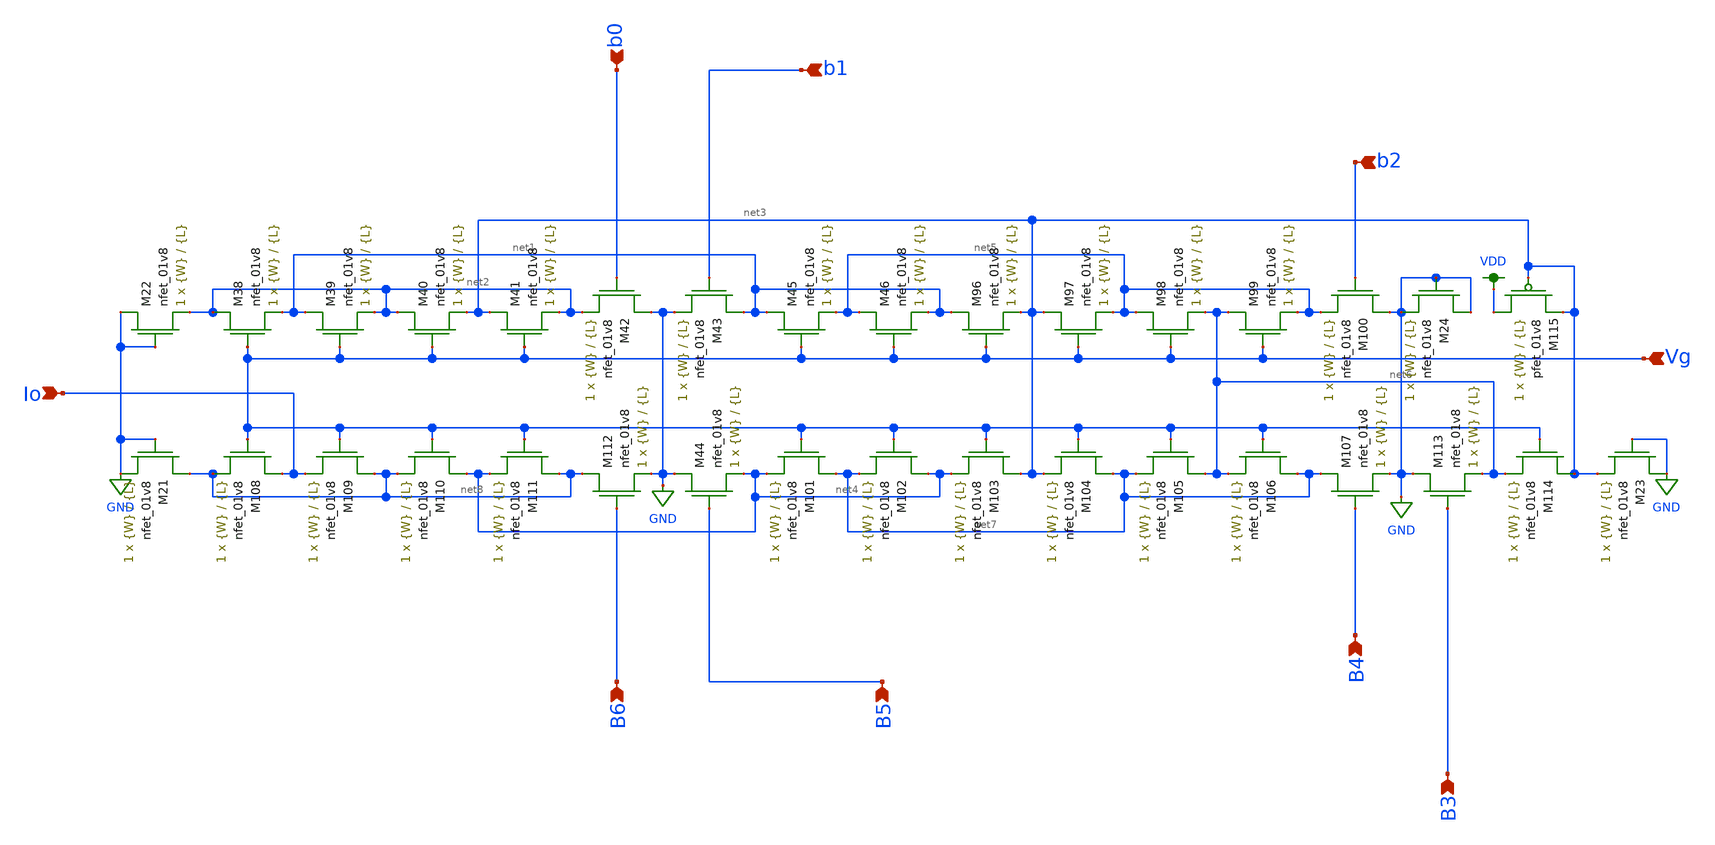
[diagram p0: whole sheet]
** sch_path: dac/schematics/misc/lvs_Dac.sch
**.subckt lvs_Dac b0 b1 b2 Vg B4 B3 B5 B6 Io
*.ipin b0
*.ipin b1
*.ipin b2
*.ipin Vg
*.ipin B4
*.ipin B3
*.ipin B5
*.ipin B6
*.ipin Io
XM38 net2 Vg net1 GND sky130_fd_pr__nfet_01v8 L={L} W={W} nf=1 ad='int((nf+1)/2) * W/nf * 0.29' as='int((nf+2)/2) * W/nf * 0.29'
+ pd='2*int((nf+1)/2) * (W/nf + 0.29)' ps='2*int((nf+2)/2) * (W/nf + 0.29)' nrd='0.29 / W' nrs='0.29 / W'
+ sa=0 sb=0 sd=0 mult=1 m=1
XM39 net1 Vg net2 GND sky130_fd_pr__nfet_01v8 L={L} W={W} nf=1 ad='int((nf+1)/2) * W/nf * 0.29' as='int((nf+2)/2) * W/nf * 0.29'
+ pd='2*int((nf+1)/2) * (W/nf + 0.29)' ps='2*int((nf+2)/2) * (W/nf + 0.29)' nrd='0.29 / W' nrs='0.29 / W'
+ sa=0 sb=0 sd=0 mult=1 m=1
XM40 net2 Vg net3 GND sky130_fd_pr__nfet_01v8 L={L} W={W} nf=1 ad='int((nf+1)/2) * W/nf * 0.29' as='int((nf+2)/2) * W/nf * 0.29'
+ pd='2*int((nf+1)/2) * (W/nf + 0.29)' ps='2*int((nf+2)/2) * (W/nf + 0.29)' nrd='0.29 / W' nrs='0.29 / W'
+ sa=0 sb=0 sd=0 mult=1 m=1
XM41 net3 Vg net2 GND sky130_fd_pr__nfet_01v8 L={L} W={W} nf=1 ad='int((nf+1)/2) * W/nf * 0.29' as='int((nf+2)/2) * W/nf * 0.29'
+ pd='2*int((nf+1)/2) * (W/nf + 0.29)' ps='2*int((nf+2)/2) * (W/nf + 0.29)' nrd='0.29 / W' nrs='0.29 / W'
+ sa=0 sb=0 sd=0 mult=1 m=1
XM42 GND b0 net2 GND sky130_fd_pr__nfet_01v8 L={L} W={W} nf=1 ad='int((nf+1)/2) * W/nf * 0.29' as='int((nf+2)/2) * W/nf * 0.29'
+ pd='2*int((nf+1)/2) * (W/nf + 0.29)' ps='2*int((nf+2)/2) * (W/nf + 0.29)' nrd='0.29 / W' nrs='0.29 / W'
+ sa=0 sb=0 sd=0 mult=1 m=1
XM43 net1 b1 GND GND sky130_fd_pr__nfet_01v8 L={L} W={W} nf=1 ad='int((nf+1)/2) * W/nf * 0.29' as='int((nf+2)/2) * W/nf * 0.29'
+ pd='2*int((nf+1)/2) * (W/nf + 0.29)' ps='2*int((nf+2)/2) * (W/nf + 0.29)' nrd='0.29 / W' nrs='0.29 / W'
+ sa=0 sb=0 sd=0 mult=1 m=1
XM44 GND B5 net4 GND sky130_fd_pr__nfet_01v8 L={L} W={W} nf=1 ad='int((nf+1)/2) * W/nf * 0.29' as='int((nf+2)/2) * W/nf * 0.29'
+ pd='2*int((nf+1)/2) * (W/nf + 0.29)' ps='2*int((nf+2)/2) * (W/nf + 0.29)' nrd='0.29 / W' nrs='0.29 / W'
+ sa=0 sb=0 sd=0 mult=1 m=1
XM45 net1 Vg net5 GND sky130_fd_pr__nfet_01v8 L={L} W={W} nf=1 ad='int((nf+1)/2) * W/nf * 0.29' as='int((nf+2)/2) * W/nf * 0.29'
+ pd='2*int((nf+1)/2) * (W/nf + 0.29)' ps='2*int((nf+2)/2) * (W/nf + 0.29)' nrd='0.29 / W' nrs='0.29 / W'
+ sa=0 sb=0 sd=0 mult=1 m=1
XM46 net5 Vg net1 GND sky130_fd_pr__nfet_01v8 L={L} W={W} nf=1 ad='int((nf+1)/2) * W/nf * 0.29' as='int((nf+2)/2) * W/nf * 0.29'
+ pd='2*int((nf+1)/2) * (W/nf + 0.29)' ps='2*int((nf+2)/2) * (W/nf + 0.29)' nrd='0.29 / W' nrs='0.29 / W'
+ sa=0 sb=0 sd=0 mult=1 m=1
XM96 net1 Vg net3 GND sky130_fd_pr__nfet_01v8 L={L} W={W} nf=1 ad='int((nf+1)/2) * W/nf * 0.29' as='int((nf+2)/2) * W/nf * 0.29'
+ pd='2*int((nf+1)/2) * (W/nf + 0.29)' ps='2*int((nf+2)/2) * (W/nf + 0.29)' nrd='0.29 / W' nrs='0.29 / W'
+ sa=0 sb=0 sd=0 mult=1 m=1
XM97 net3 Vg net5 GND sky130_fd_pr__nfet_01v8 L={L} W={W} nf=1 ad='int((nf+1)/2) * W/nf * 0.29' as='int((nf+2)/2) * W/nf * 0.29'
+ pd='2*int((nf+1)/2) * (W/nf + 0.29)' ps='2*int((nf+2)/2) * (W/nf + 0.29)' nrd='0.29 / W' nrs='0.29 / W'
+ sa=0 sb=0 sd=0 mult=1 m=1
XM98 net5 Vg net6 GND sky130_fd_pr__nfet_01v8 L={L} W={W} nf=1 ad='int((nf+1)/2) * W/nf * 0.29' as='int((nf+2)/2) * W/nf * 0.29'
+ pd='2*int((nf+1)/2) * (W/nf + 0.29)' ps='2*int((nf+2)/2) * (W/nf + 0.29)' nrd='0.29 / W' nrs='0.29 / W'
+ sa=0 sb=0 sd=0 mult=1 m=1
XM99 net6 Vg net5 GND sky130_fd_pr__nfet_01v8 L={L} W={W} nf=1 ad='int((nf+1)/2) * W/nf * 0.29' as='int((nf+2)/2) * W/nf * 0.29'
+ pd='2*int((nf+1)/2) * (W/nf + 0.29)' ps='2*int((nf+2)/2) * (W/nf + 0.29)' nrd='0.29 / W' nrs='0.29 / W'
+ sa=0 sb=0 sd=0 mult=1 m=1
XM100 GND b2 net5 GND sky130_fd_pr__nfet_01v8 L={L} W={W} nf=1 ad='int((nf+1)/2) * W/nf * 0.29' as='int((nf+2)/2) * W/nf * 0.29'
+ pd='2*int((nf+1)/2) * (W/nf + 0.29)' ps='2*int((nf+2)/2) * (W/nf + 0.29)' nrd='0.29 / W' nrs='0.29 / W'
+ sa=0 sb=0 sd=0 mult=1 m=1
XM101 net7 Vg net4 GND sky130_fd_pr__nfet_01v8 L={L} W={W} nf=1 ad='int((nf+1)/2) * W/nf * 0.29' as='int((nf+2)/2) * W/nf * 0.29'
+ pd='2*int((nf+1)/2) * (W/nf + 0.29)' ps='2*int((nf+2)/2) * (W/nf + 0.29)' nrd='0.29 / W' nrs='0.29 / W'
+ sa=0 sb=0 sd=0 mult=1 m=1
XM102 net4 Vg net7 GND sky130_fd_pr__nfet_01v8 L={L} W={W} nf=1 ad='int((nf+1)/2) * W/nf * 0.29' as='int((nf+2)/2) * W/nf * 0.29'
+ pd='2*int((nf+1)/2) * (W/nf + 0.29)' ps='2*int((nf+2)/2) * (W/nf + 0.29)' nrd='0.29 / W' nrs='0.29 / W'
+ sa=0 sb=0 sd=0 mult=1 m=1
XM103 net3 Vg net4 GND sky130_fd_pr__nfet_01v8 L={L} W={W} nf=1 ad='int((nf+1)/2) * W/nf * 0.29' as='int((nf+2)/2) * W/nf * 0.29'
+ pd='2*int((nf+1)/2) * (W/nf + 0.29)' ps='2*int((nf+2)/2) * (W/nf + 0.29)' nrd='0.29 / W' nrs='0.29 / W'
+ sa=0 sb=0 sd=0 mult=1 m=1
XM104 net7 Vg net3 GND sky130_fd_pr__nfet_01v8 L={L} W={W} nf=1 ad='int((nf+1)/2) * W/nf * 0.29' as='int((nf+2)/2) * W/nf * 0.29'
+ pd='2*int((nf+1)/2) * (W/nf + 0.29)' ps='2*int((nf+2)/2) * (W/nf + 0.29)' nrd='0.29 / W' nrs='0.29 / W'
+ sa=0 sb=0 sd=0 mult=1 m=1
XM105 net6 Vg net7 GND sky130_fd_pr__nfet_01v8 L={L} W={W} nf=1 ad='int((nf+1)/2) * W/nf * 0.29' as='int((nf+2)/2) * W/nf * 0.29'
+ pd='2*int((nf+1)/2) * (W/nf + 0.29)' ps='2*int((nf+2)/2) * (W/nf + 0.29)' nrd='0.29 / W' nrs='0.29 / W'
+ sa=0 sb=0 sd=0 mult=1 m=1
XM106 net7 Vg net6 GND sky130_fd_pr__nfet_01v8 L={L} W={W} nf=1 ad='int((nf+1)/2) * W/nf * 0.29' as='int((nf+2)/2) * W/nf * 0.29'
+ pd='2*int((nf+1)/2) * (W/nf + 0.29)' ps='2*int((nf+2)/2) * (W/nf + 0.29)' nrd='0.29 / W' nrs='0.29 / W'
+ sa=0 sb=0 sd=0 mult=1 m=1
XM107 net7 B4 GND GND sky130_fd_pr__nfet_01v8 L={L} W={W} nf=1 ad='int((nf+1)/2) * W/nf * 0.29' as='int((nf+2)/2) * W/nf * 0.29'
+ pd='2*int((nf+1)/2) * (W/nf + 0.29)' ps='2*int((nf+2)/2) * (W/nf + 0.29)' nrd='0.29 / W' nrs='0.29 / W'
+ sa=0 sb=0 sd=0 mult=1 m=1
XM108 Io Vg net8 GND sky130_fd_pr__nfet_01v8 L={L} W={W} nf=1 ad='int((nf+1)/2) * W/nf * 0.29' as='int((nf+2)/2) * W/nf * 0.29'
+ pd='2*int((nf+1)/2) * (W/nf + 0.29)' ps='2*int((nf+2)/2) * (W/nf + 0.29)' nrd='0.29 / W' nrs='0.29 / W'
+ sa=0 sb=0 sd=0 mult=1 m=1
XM109 net8 Vg Io GND sky130_fd_pr__nfet_01v8 L={L} W={W} nf=1 ad='int((nf+1)/2) * W/nf * 0.29' as='int((nf+2)/2) * W/nf * 0.29'
+ pd='2*int((nf+1)/2) * (W/nf + 0.29)' ps='2*int((nf+2)/2) * (W/nf + 0.29)' nrd='0.29 / W' nrs='0.29 / W'
+ sa=0 sb=0 sd=0 mult=1 m=1
XM110 net4 Vg net8 GND sky130_fd_pr__nfet_01v8 L={L} W={W} nf=1 ad='int((nf+1)/2) * W/nf * 0.29' as='int((nf+2)/2) * W/nf * 0.29'
+ pd='2*int((nf+1)/2) * (W/nf + 0.29)' ps='2*int((nf+2)/2) * (W/nf + 0.29)' nrd='0.29 / W' nrs='0.29 / W'
+ sa=0 sb=0 sd=0 mult=1 m=1
XM111 net8 Vg net4 GND sky130_fd_pr__nfet_01v8 L={L} W={W} nf=1 ad='int((nf+1)/2) * W/nf * 0.29' as='int((nf+2)/2) * W/nf * 0.29'
+ pd='2*int((nf+1)/2) * (W/nf + 0.29)' ps='2*int((nf+2)/2) * (W/nf + 0.29)' nrd='0.29 / W' nrs='0.29 / W'
+ sa=0 sb=0 sd=0 mult=1 m=1
XM112 net8 B6 GND GND sky130_fd_pr__nfet_01v8 L={L} W={W} nf=1 ad='int((nf+1)/2) * W/nf * 0.29' as='int((nf+2)/2) * W/nf * 0.29'
+ pd='2*int((nf+1)/2) * (W/nf + 0.29)' ps='2*int((nf+2)/2) * (W/nf + 0.29)' nrd='0.29 / W' nrs='0.29 / W'
+ sa=0 sb=0 sd=0 mult=1 m=1
XM113 GND B3 net6 GND sky130_fd_pr__nfet_01v8 L={L} W={W} nf=1 ad='int((nf+1)/2) * W/nf * 0.29' as='int((nf+2)/2) * W/nf * 0.29'
+ pd='2*int((nf+1)/2) * (W/nf + 0.29)' ps='2*int((nf+2)/2) * (W/nf + 0.29)' nrd='0.29 / W' nrs='0.29 / W'
+ sa=0 sb=0 sd=0 mult=1 m=1
XM114 net3 Vg net6 GND sky130_fd_pr__nfet_01v8 L={L} W={W} nf=1 ad='int((nf+1)/2) * W/nf * 0.29' as='int((nf+2)/2) * W/nf * 0.29'
+ pd='2*int((nf+1)/2) * (W/nf + 0.29)' ps='2*int((nf+2)/2) * (W/nf + 0.29)' nrd='0.29 / W' nrs='0.29 / W'
+ sa=0 sb=0 sd=0 mult=1 m=1
XM115 VDD net3 net3 VDD sky130_fd_pr__pfet_01v8 L={L} W={W} nf=1 ad='int((nf+1)/2) * W/nf * 0.29' as='int((nf+2)/2) * W/nf * 0.29'
+ pd='2*int((nf+1)/2) * (W/nf + 0.29)' ps='2*int((nf+2)/2) * (W/nf + 0.29)' nrd='0.29 / W' nrs='0.29 / W'
+ sa=0 sb=0 sd=0 mult=1 m=1
XM21 net8 GND GND GND sky130_fd_pr__nfet_01v8 L={L} W={W} nf=1 ad='int((nf+1)/2) * W/nf * 0.29' as='int((nf+2)/2) * W/nf * 0.29'
+ pd='2*int((nf+1)/2) * (W/nf + 0.29)' ps='2*int((nf+2)/2) * (W/nf + 0.29)' nrd='0.29 / W' nrs='0.29 / W'
+ sa=0 sb=0 sd=0 mult=1 m=1
XM22 GND GND net2 GND sky130_fd_pr__nfet_01v8 L={L} W={W} nf=1 ad='int((nf+1)/2) * W/nf * 0.29' as='int((nf+2)/2) * W/nf * 0.29'
+ pd='2*int((nf+1)/2) * (W/nf + 0.29)' ps='2*int((nf+2)/2) * (W/nf + 0.29)' nrd='0.29 / W' nrs='0.29 / W'
+ sa=0 sb=0 sd=0 mult=1 m=1
XM23 GND GND net3 GND sky130_fd_pr__nfet_01v8 L={L} W={W} nf=1 ad='int((nf+1)/2) * W/nf * 0.29' as='int((nf+2)/2) * W/nf * 0.29'
+ pd='2*int((nf+1)/2) * (W/nf + 0.29)' ps='2*int((nf+2)/2) * (W/nf + 0.29)' nrd='0.29 / W' nrs='0.29 / W'
+ sa=0 sb=0 sd=0 mult=1 m=1
XM24 GND GND GND GND sky130_fd_pr__nfet_01v8 L={L} W={W} nf=1 ad='int((nf+1)/2) * W/nf * 0.29' as='int((nf+2)/2) * W/nf * 0.29'
+ pd='2*int((nf+1)/2) * (W/nf + 0.29)' ps='2*int((nf+2)/2) * (W/nf + 0.29)' nrd='0.29 / W' nrs='0.29 / W'
+ sa=0 sb=0 sd=0 mult=1 m=1
**** begin user architecture code

.param W=24
.param L=1
.control
set wr_vecnames
set wr_singlescale
let code = 0
  while code < 128
    if code eq 0
      let b0 = 0
    else
      let b0 = code % 2 * 1.8
    end
    if floor(code / 2) eq 0
      let b1 = 0
    else
      let b1 = floor(code / 2) % 2 * 1.8
    end
    if floor(code / 4) eq 0
      let b2 = 0
    else
      let b2 = floor(code / 4) % 2 * 1.8
    end
    if floor(code / 8) eq 0
      let b3 = 0
    else
      let b3 = floor(code / 8) % 2 * 1.8
    end
    if floor(code / 16) eq 0
      let b4 = 0
    else
      let b4 = floor(code / 16) % 2 * 1.8
    end
    if floor(code / 32) eq 0
      let b5 = 0
    else
      let b5 = floor(code / 32) % 2 * 1.8
    end
    if floor(code / 64) eq 0
      let b6 = 0
    else
      let b6 = floor(code / 64) % 2 * 1.8
    end
    alter v0 $&b0
    alter v1 $&b1
    alter v2 $&b2
    alter v3 $&b3
    alter v4 $&b4
    alter v5 $&b5
    alter v6 $&b6
    save all
    op
    wrdata ~/Documents/current-output-dac-vlsi/simulations/dac_sim.txt i(Vout)
    if code eq 0
      set appendwrite
      set wr_vecnames = FALSE
    end
    let code = code + 1
  end
.endc

**** end user architecture code
**.ends
.GLOBAL GND
.GLOBAL VDD
.end
